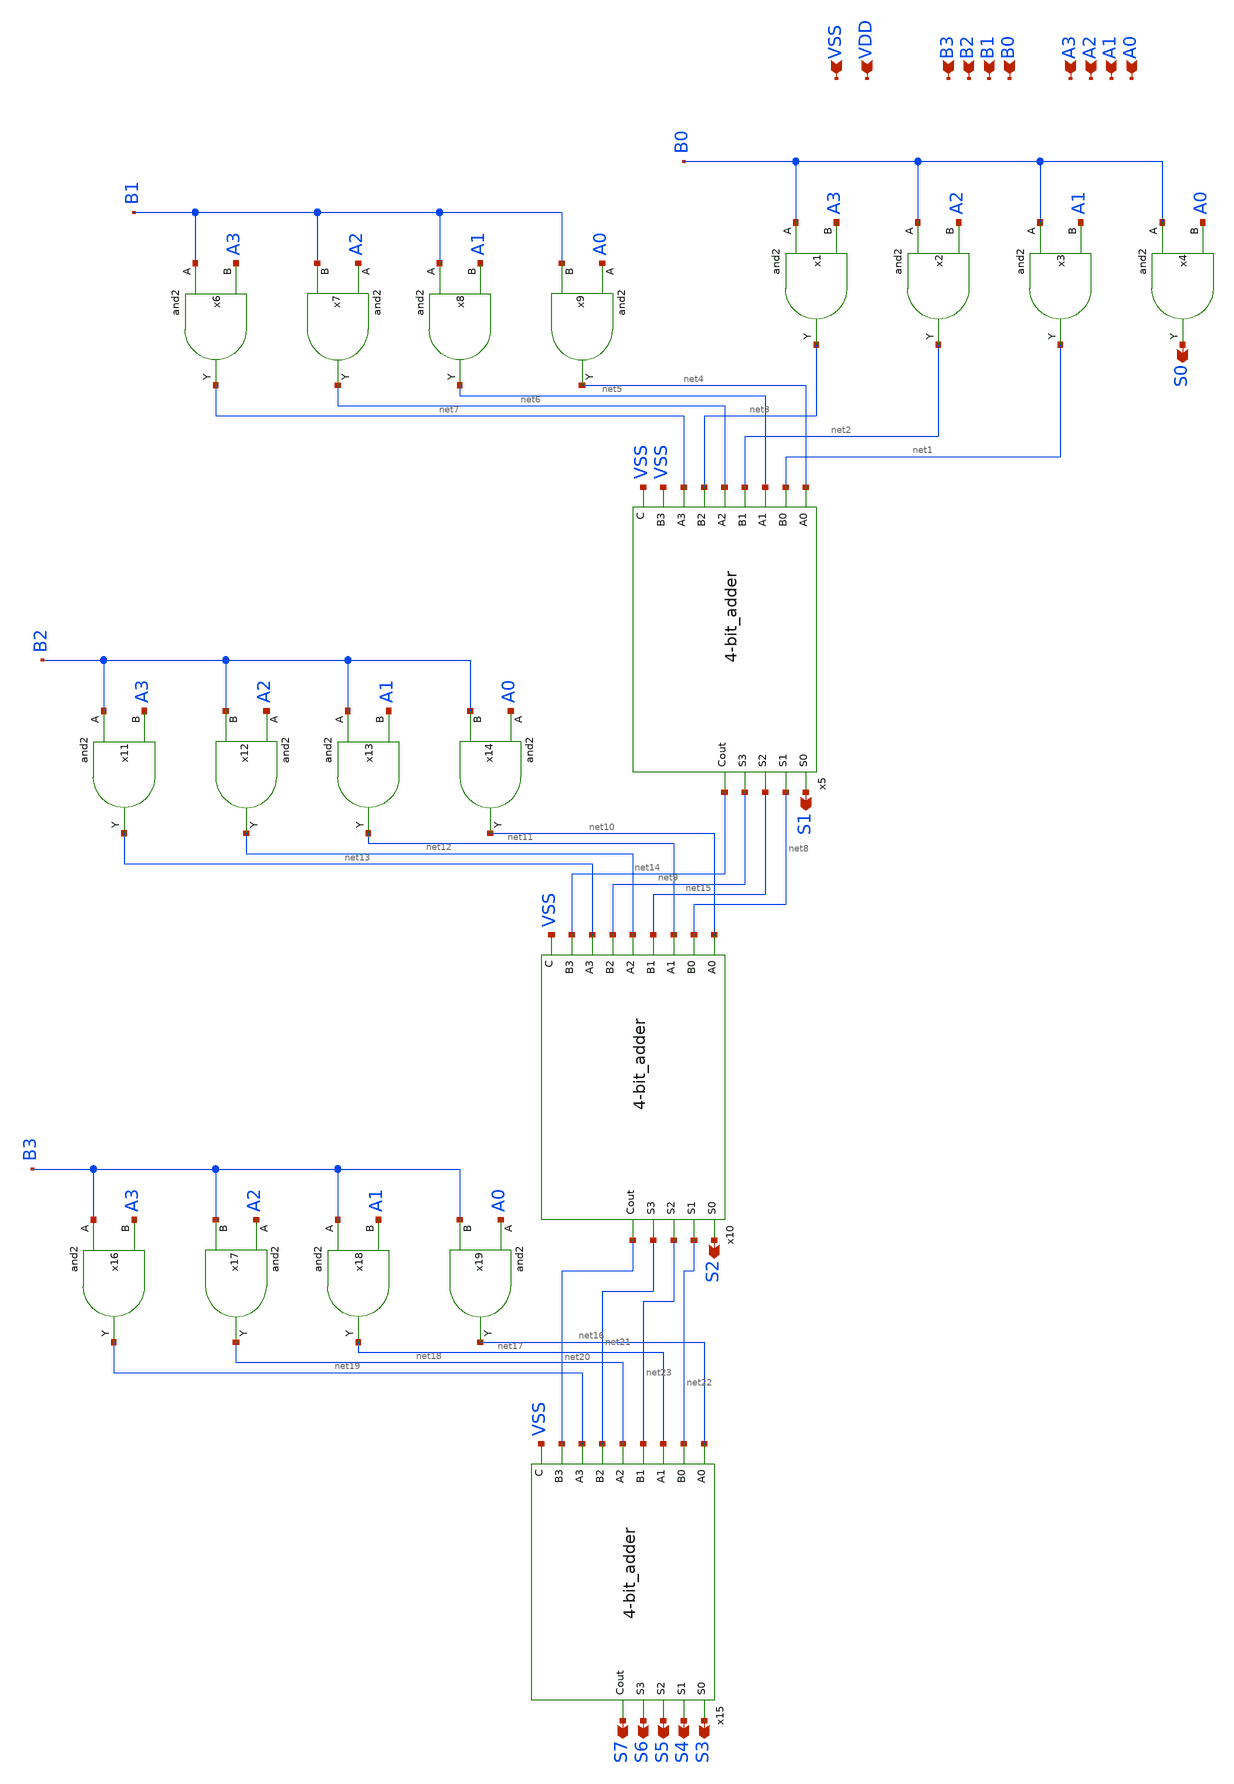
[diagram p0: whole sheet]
** sch_path: design/xschem/MULTIPLIER/mul.sch
**.subckt mul A0 A1 A2 A3 B1 B2 B3 B0 S6 S7 S3 S4 S5 S0 S1 S2 VSS VDD
*.ipin A0
*.ipin A1
*.ipin A2
*.ipin A3
*.ipin B1
*.ipin B2
*.ipin B3
*.ipin B0
*.opin S6
*.opin S7
*.opin S3
*.opin S4
*.opin S5
*.opin S0
*.opin S1
*.opin S2
*.ipin VSS
*.ipin VDD
x1 B0 A3 VSS VDD net3 and2
x2 B0 A2 VSS VDD net2 and2
x3 B0 A1 VSS VDD net1 and2
x4 B0 A0 VSS VDD S0 and2
x5 net4 S1 net1 net5 net8 net2 net6 net15 net3 net7 net9 VSS net14 VSS 4-bit_adder
x6 B1 A3 VSS VDD net7 and2
x7 A2 B1 VSS VDD net6 and2
x8 B1 A1 VSS VDD net5 and2
x9 A0 B1 VSS VDD net4 and2
x10 net10 S2 net8 net11 net22 net15 net12 net23 net9 net13 net21 net14 net20 VSS 4-bit_adder
x11 B2 A3 VSS VDD net13 and2
x12 A2 B2 VSS VDD net12 and2
x13 B2 A1 VSS VDD net11 and2
x14 A0 B2 VSS VDD net10 and2
x15 net16 S3 net22 net17 S4 net23 net18 S5 net21 net19 S6 net20 S7 VSS 4-bit_adder
x16 B3 A3 VSS VDD net19 and2
x17 A2 B3 VSS VDD net18 and2
x18 B3 A1 VSS VDD net17 and2
x19 A0 B3 VSS VDD net16 and2
**.ends
.end
